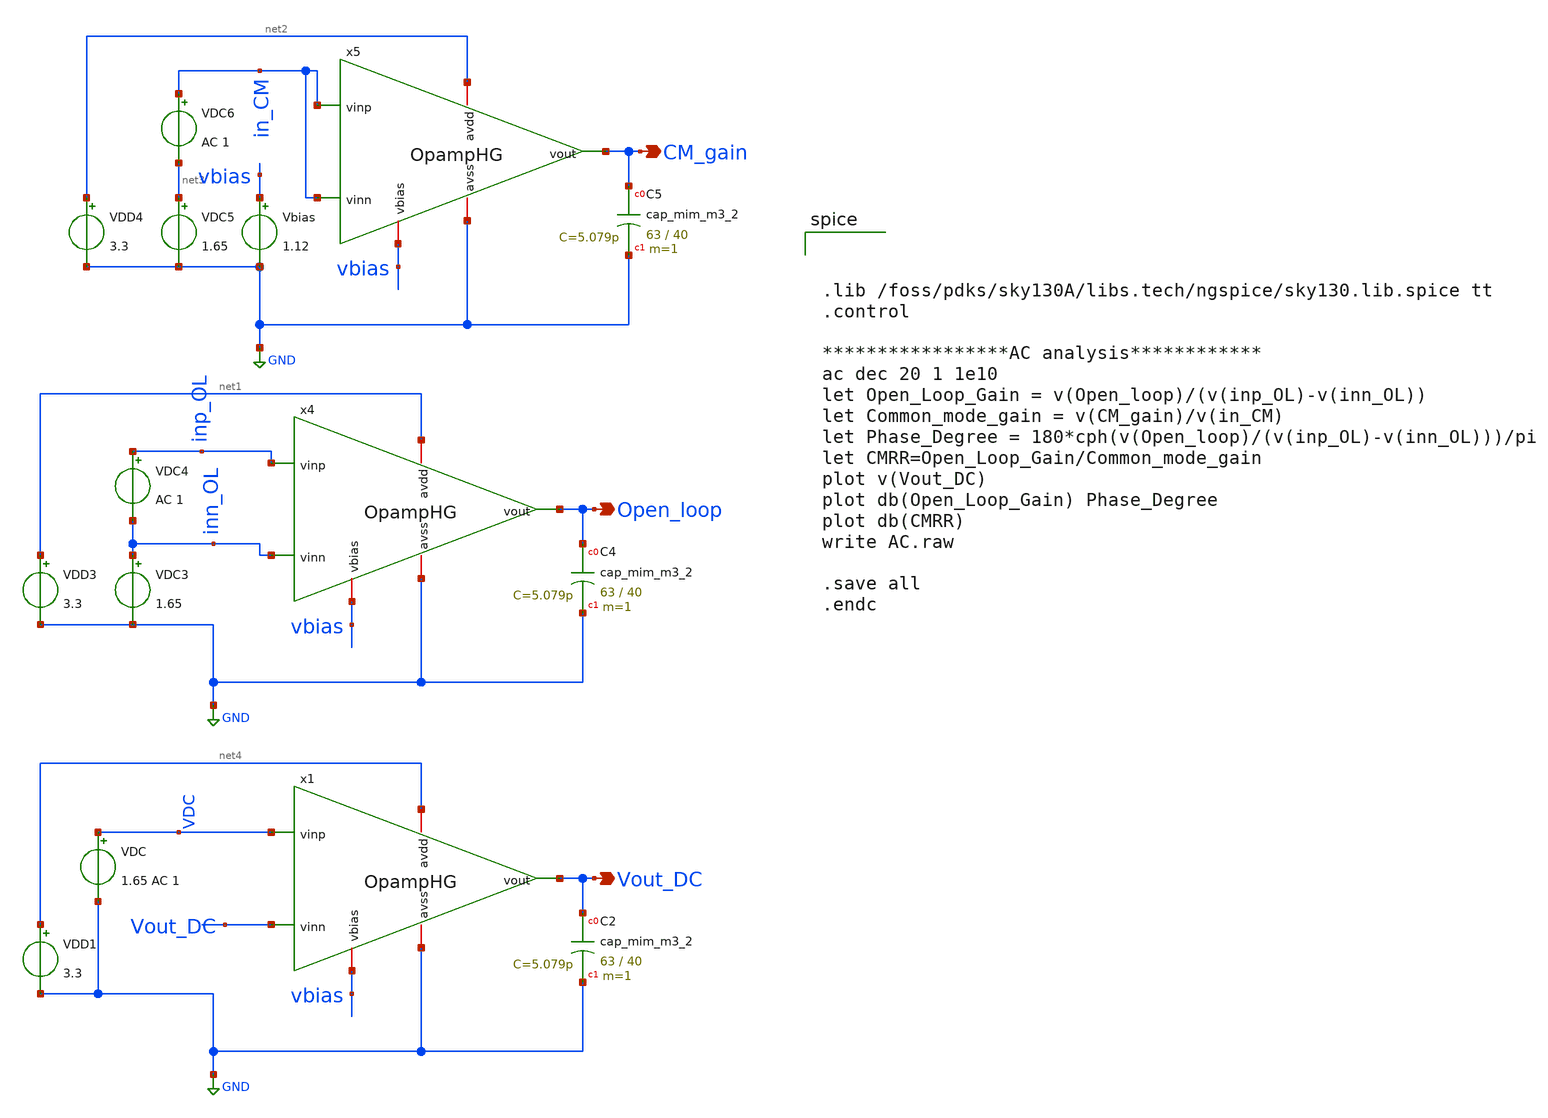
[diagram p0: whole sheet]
** sch_path: OpampHG_AC.sch
**.subckt OpampHG_AC Open_loop CM_gain Vout_DC
*.opin Open_loop
*.opin CM_gain
*.opin Vout_DC
x4 net1 GND vbias inp_OL inn_OL Open_loop OpampHG
VDD3 net1 GND 3.3
VDC3 inn_OL GND 1.65
XC4 Open_loop GND sky130_fd_pr__cap_mim_m3_2 W=63 L=40 MF=1 m=1
VDC4 inp_OL inn_OL AC 1
x5 net2 GND vbias in_CM in_CM CM_gain OpampHG
VDD4 net2 GND 3.3
VDC5 net3 GND 1.65
XC5 CM_gain GND sky130_fd_pr__cap_mim_m3_2 W=63 L=40 MF=1 m=1
VDC6 in_CM net3 AC 1
Vbias vbias GND 1.12
x1 net4 GND vbias VDC Vout_DC Vout_DC OpampHG
VDD1 net4 GND 3.3
VDC VDC GND 1.65 AC 1
XC2 Vout_DC GND sky130_fd_pr__cap_mim_m3_2 W=63 L=40 MF=1 m=1
**** begin user architecture code



.lib /foss/pdks/sky130A/libs.tech/ngspice/sky130.lib.spice tt
.control

*****************AC analysis************
ac dec 20 1 1e10
let Open_Loop_Gain = v(Open_loop)/(v(inp_OL)-v(inn_OL))
let Common_mode_gain = v(CM_gain)/v(in_CM)
let Phase_Degree = 180*cph(v(Open_loop)/(v(inp_OL)-v(inn_OL)))/pi
let CMRR=Open_Loop_Gain/Common_mode_gain
plot v(Vout_DC)
plot db(Open_Loop_Gain) Phase_Degree
plot db(CMRR)
write AC.raw

.save all
.endc


**** end user architecture code
**.ends

* expanding   symbol:  /foss/designs/Opamp_HG/OpampHG.sym # of pins=6
** sym_path: OpampHG.sym
** sch_path: OpampHG.sch
.subckt OpampHG avdd avss vbias vinp vinn vout
*.iopin avdd
*.iopin avss
*.iopin vbias
*.ipin vinp
*.ipin vinn
*.opin vout
XC1 net2 Vout_prior sky130_fd_pr__cap_mim_m3_1 W=13 L=9.9 MF=1 m=1
XC2 net3 vout sky130_fd_pr__cap_mim_m3_2 W=20 L=37 MF=1 m=1
XM1 net1 net2 avdd avdd sky130_fd_pr__pfet_01v8 L=0.3 W=5 nf=1 ad='int((nf+1)/2) * W/nf * 0.29' as='int((nf+2)/2) * W/nf * 0.29'
+ pd='2*int((nf+1)/2) * (W/nf + 0.29)' ps='2*int((nf+2)/2) * (W/nf + 0.29)' nrd='0.29 / W' nrs='0.29 / W'
+ sa=0 sb=0 sd=0 mult=1 m=1
XM2 net3 net2 avdd avdd sky130_fd_pr__pfet_01v8 L=0.3 W=5 nf=1 ad='int((nf+1)/2) * W/nf * 0.29' as='int((nf+2)/2) * W/nf * 0.29'
+ pd='2*int((nf+1)/2) * (W/nf + 0.29)' ps='2*int((nf+2)/2) * (W/nf + 0.29)' nrd='0.29 / W' nrs='0.29 / W'
+ sa=0 sb=0 sd=0 mult=1 m=1
XM3 net2 net2 net1 avdd sky130_fd_pr__pfet_01v8 L=0.3 W=5 nf=1 ad='int((nf+1)/2) * W/nf * 0.29' as='int((nf+2)/2) * W/nf * 0.29'
+ pd='2*int((nf+1)/2) * (W/nf + 0.29)' ps='2*int((nf+2)/2) * (W/nf + 0.29)' nrd='0.29 / W' nrs='0.29 / W'
+ sa=0 sb=0 sd=0 mult=1 m=1
XM4 net5 net2 net3 avdd sky130_fd_pr__pfet_01v8 L=0.3 W=5 nf=1 ad='int((nf+1)/2) * W/nf * 0.29' as='int((nf+2)/2) * W/nf * 0.29'
+ pd='2*int((nf+1)/2) * (W/nf + 0.29)' ps='2*int((nf+2)/2) * (W/nf + 0.29)' nrd='0.29 / W' nrs='0.29 / W'
+ sa=0 sb=0 sd=0 mult=1 m=1
XM5 net7 net6 avdd avdd sky130_fd_pr__pfet_01v8 L=0.3 W=5 nf=1 ad='int((nf+1)/2) * W/nf * 0.29' as='int((nf+2)/2) * W/nf * 0.29'
+ pd='2*int((nf+1)/2) * (W/nf + 0.29)' ps='2*int((nf+2)/2) * (W/nf + 0.29)' nrd='0.29 / W' nrs='0.29 / W'
+ sa=0 sb=0 sd=0 mult=1 m=1
XM6 net8 net6 avdd avdd sky130_fd_pr__pfet_01v8 L=0.3 W=5 nf=1 ad='int((nf+1)/2) * W/nf * 0.29' as='int((nf+2)/2) * W/nf * 0.29'
+ pd='2*int((nf+1)/2) * (W/nf + 0.29)' ps='2*int((nf+2)/2) * (W/nf + 0.29)' nrd='0.29 / W' nrs='0.29 / W'
+ sa=0 sb=0 sd=0 mult=1 m=1
XM7 net6 net6 net7 avdd sky130_fd_pr__pfet_01v8 L=0.3 W=5 nf=1 ad='int((nf+1)/2) * W/nf * 0.29' as='int((nf+2)/2) * W/nf * 0.29'
+ pd='2*int((nf+1)/2) * (W/nf + 0.29)' ps='2*int((nf+2)/2) * (W/nf + 0.29)' nrd='0.29 / W' nrs='0.29 / W'
+ sa=0 sb=0 sd=0 mult=1 m=1
XM8 Vout_prior net6 net8 avdd sky130_fd_pr__pfet_01v8 L=0.3 W=5 nf=1 ad='int((nf+1)/2) * W/nf * 0.29'
+ as='int((nf+2)/2) * W/nf * 0.29' pd='2*int((nf+1)/2) * (W/nf + 0.29)' ps='2*int((nf+2)/2) * (W/nf + 0.29)'
+ nrd='0.29 / W' nrs='0.29 / W' sa=0 sb=0 sd=0 mult=1 m=1
XM9 net11 Vout_prior avdd avdd sky130_fd_pr__pfet_01v8 L=0.3 W=50 nf=1 ad='int((nf+1)/2) * W/nf * 0.29'
+ as='int((nf+2)/2) * W/nf * 0.29' pd='2*int((nf+1)/2) * (W/nf + 0.29)' ps='2*int((nf+2)/2) * (W/nf + 0.29)'
+ nrd='0.29 / W' nrs='0.29 / W' sa=0 sb=0 sd=0 mult=1 m=1
XM10 vout Vout_prior net11 avdd sky130_fd_pr__pfet_01v8 L=0.3 W=50 nf=1 ad='int((nf+1)/2) * W/nf * 0.29'
+ as='int((nf+2)/2) * W/nf * 0.29' pd='2*int((nf+1)/2) * (W/nf + 0.29)' ps='2*int((nf+2)/2) * (W/nf + 0.29)'
+ nrd='0.29 / W' nrs='0.29 / W' sa=0 sb=0 sd=0 mult=1 m=1
XM11 net2 vinn net4 avss sky130_fd_pr__nfet_01v8 L=2 W=5 nf=1 ad='int((nf+1)/2) * W/nf * 0.29' as='int((nf+2)/2) * W/nf * 0.29'
+ pd='2*int((nf+1)/2) * (W/nf + 0.29)' ps='2*int((nf+2)/2) * (W/nf + 0.29)' nrd='0.29 / W' nrs='0.29 / W'
+ sa=0 sb=0 sd=0 mult=1 m=1
XM12 net5 vinp net4 avss sky130_fd_pr__nfet_01v8 L=2 W=5 nf=1 ad='int((nf+1)/2) * W/nf * 0.29' as='int((nf+2)/2) * W/nf * 0.29'
+ pd='2*int((nf+1)/2) * (W/nf + 0.29)' ps='2*int((nf+2)/2) * (W/nf + 0.29)' nrd='0.29 / W' nrs='0.29 / W'
+ sa=0 sb=0 sd=0 mult=1 m=1
XM13 net6 net5 net10 avss sky130_fd_pr__nfet_01v8 L=2 W=5 nf=1 ad='int((nf+1)/2) * W/nf * 0.29' as='int((nf+2)/2) * W/nf * 0.29'
+ pd='2*int((nf+1)/2) * (W/nf + 0.29)' ps='2*int((nf+2)/2) * (W/nf + 0.29)' nrd='0.29 / W' nrs='0.29 / W'
+ sa=0 sb=0 sd=0 mult=1 m=1
XM14 Vout_prior net2 net9 avss sky130_fd_pr__nfet_01v8 L=2 W=5 nf=1 ad='int((nf+1)/2) * W/nf * 0.29'
+ as='int((nf+2)/2) * W/nf * 0.29' pd='2*int((nf+1)/2) * (W/nf + 0.29)' ps='2*int((nf+2)/2) * (W/nf + 0.29)'
+ nrd='0.29 / W' nrs='0.29 / W' sa=0 sb=0 sd=0 mult=1 m=1
XM15 net4 vbias avss avss sky130_fd_pr__nfet_01v8 L=0.6 W=2.6 nf=1 ad='int((nf+1)/2) * W/nf * 0.29' as='int((nf+2)/2) * W/nf * 0.29'
+ pd='2*int((nf+1)/2) * (W/nf + 0.29)' ps='2*int((nf+2)/2) * (W/nf + 0.29)' nrd='0.29 / W' nrs='0.29 / W'
+ sa=0 sb=0 sd=0 mult=1 m=1
XM16 net4 vbias avss avss sky130_fd_pr__nfet_01v8 L=0.6 W=2.6 nf=1 ad='int((nf+1)/2) * W/nf * 0.29' as='int((nf+2)/2) * W/nf * 0.29'
+ pd='2*int((nf+1)/2) * (W/nf + 0.29)' ps='2*int((nf+2)/2) * (W/nf + 0.29)' nrd='0.29 / W' nrs='0.29 / W'
+ sa=0 sb=0 sd=0 mult=1 m=1
XM17 net10 vbias avss avss sky130_fd_pr__nfet_01v8 L=0.6 W=2.6 nf=1 ad='int((nf+1)/2) * W/nf * 0.29'
+ as='int((nf+2)/2) * W/nf * 0.29' pd='2*int((nf+1)/2) * (W/nf + 0.29)' ps='2*int((nf+2)/2) * (W/nf + 0.29)'
+ nrd='0.29 / W' nrs='0.29 / W' sa=0 sb=0 sd=0 mult=1 m=1
XM18 net9 vbias avss avss sky130_fd_pr__nfet_01v8 L=0.6 W=2.6 nf=1 ad='int((nf+1)/2) * W/nf * 0.29' as='int((nf+2)/2) * W/nf * 0.29'
+ pd='2*int((nf+1)/2) * (W/nf + 0.29)' ps='2*int((nf+2)/2) * (W/nf + 0.29)' nrd='0.29 / W' nrs='0.29 / W'
+ sa=0 sb=0 sd=0 mult=1 m=1
XM19 vout vbias avss avss sky130_fd_pr__nfet_01v8 L=0.6 W=20.4 nf=1 ad='int((nf+1)/2) * W/nf * 0.29'
+ as='int((nf+2)/2) * W/nf * 0.29' pd='2*int((nf+1)/2) * (W/nf + 0.29)' ps='2*int((nf+2)/2) * (W/nf + 0.29)'
+ nrd='0.29 / W' nrs='0.29 / W' sa=0 sb=0 sd=0 mult=1 m=1
.ends

.GLOBAL GND
.end
